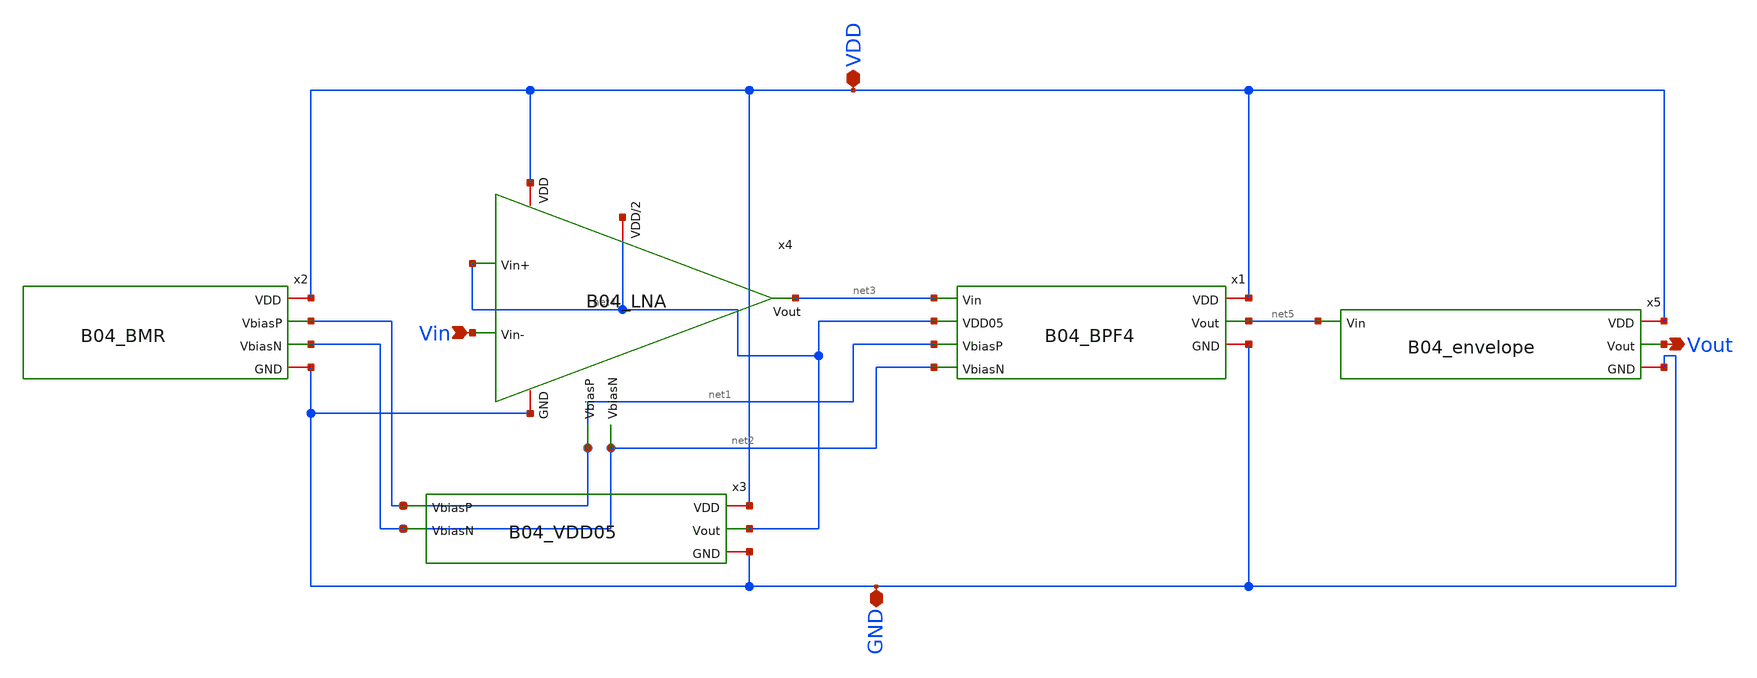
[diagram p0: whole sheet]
** sch_path: analog/B04_TOP.sch
**.subckt B04_TOP Vin VDD GND Vout
*.ipin Vin
*.iopin VDD
*.iopin GND
*.opin Vout
x1 VDD net3 net5 net4 net1 net2 GND B04_BPF4
x2 VDD net1 net2 GND B04_BMR
x3 VDD net4 GND net1 net2 B04_VDD05
x4 VDD net4 net4 net3 Vin GND net1 net2 B04_LNA
x5 VDD net5 Vout GND B04_envelope
**.ends
.end
